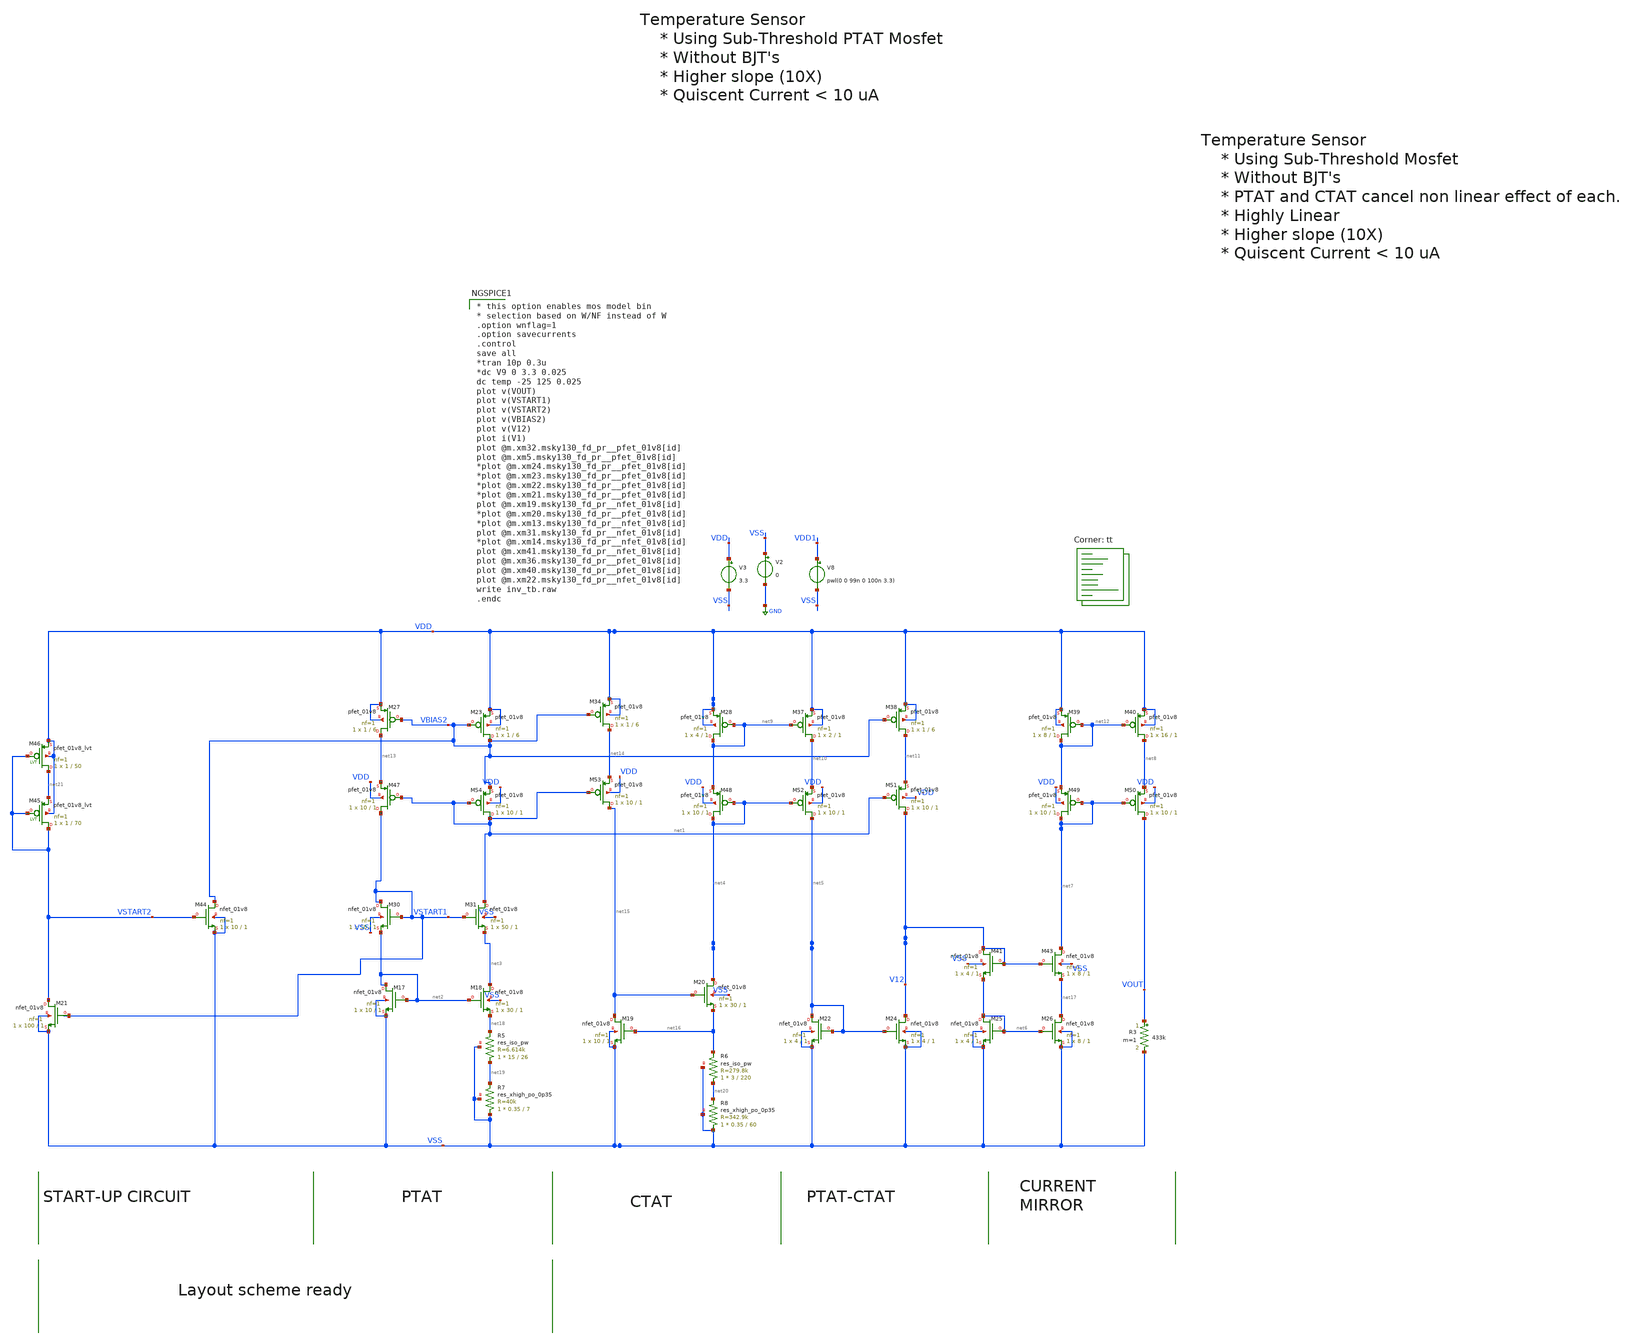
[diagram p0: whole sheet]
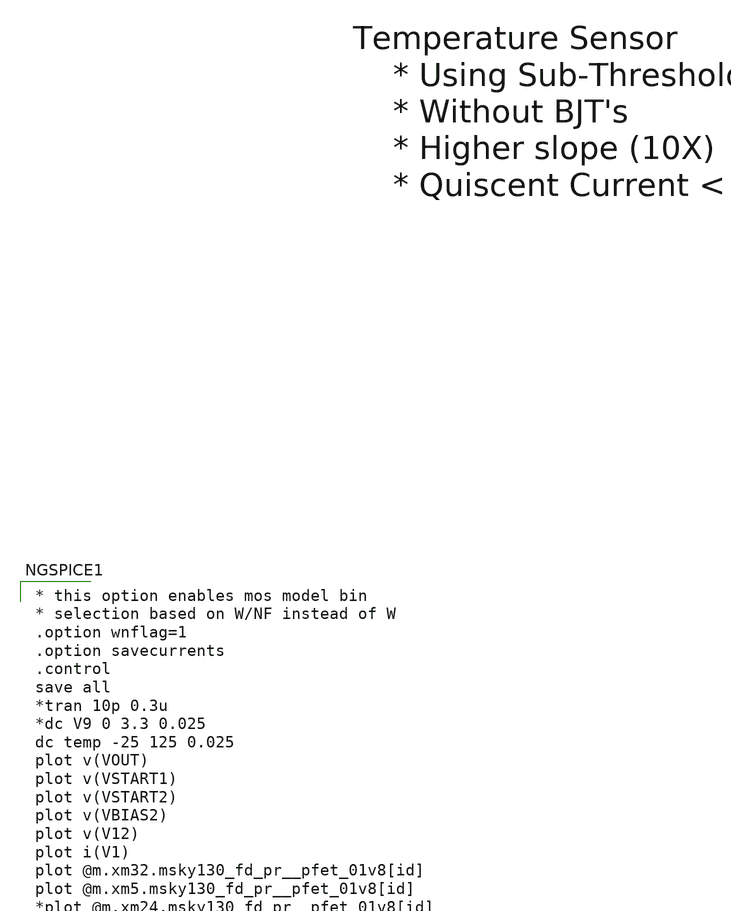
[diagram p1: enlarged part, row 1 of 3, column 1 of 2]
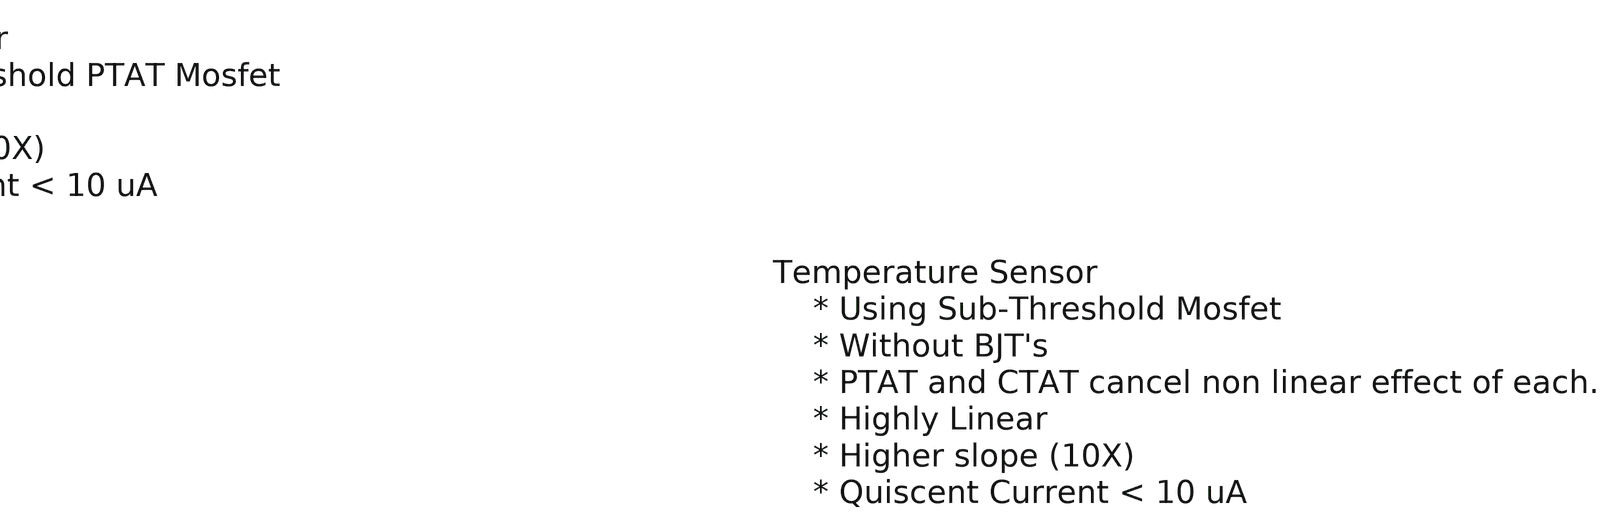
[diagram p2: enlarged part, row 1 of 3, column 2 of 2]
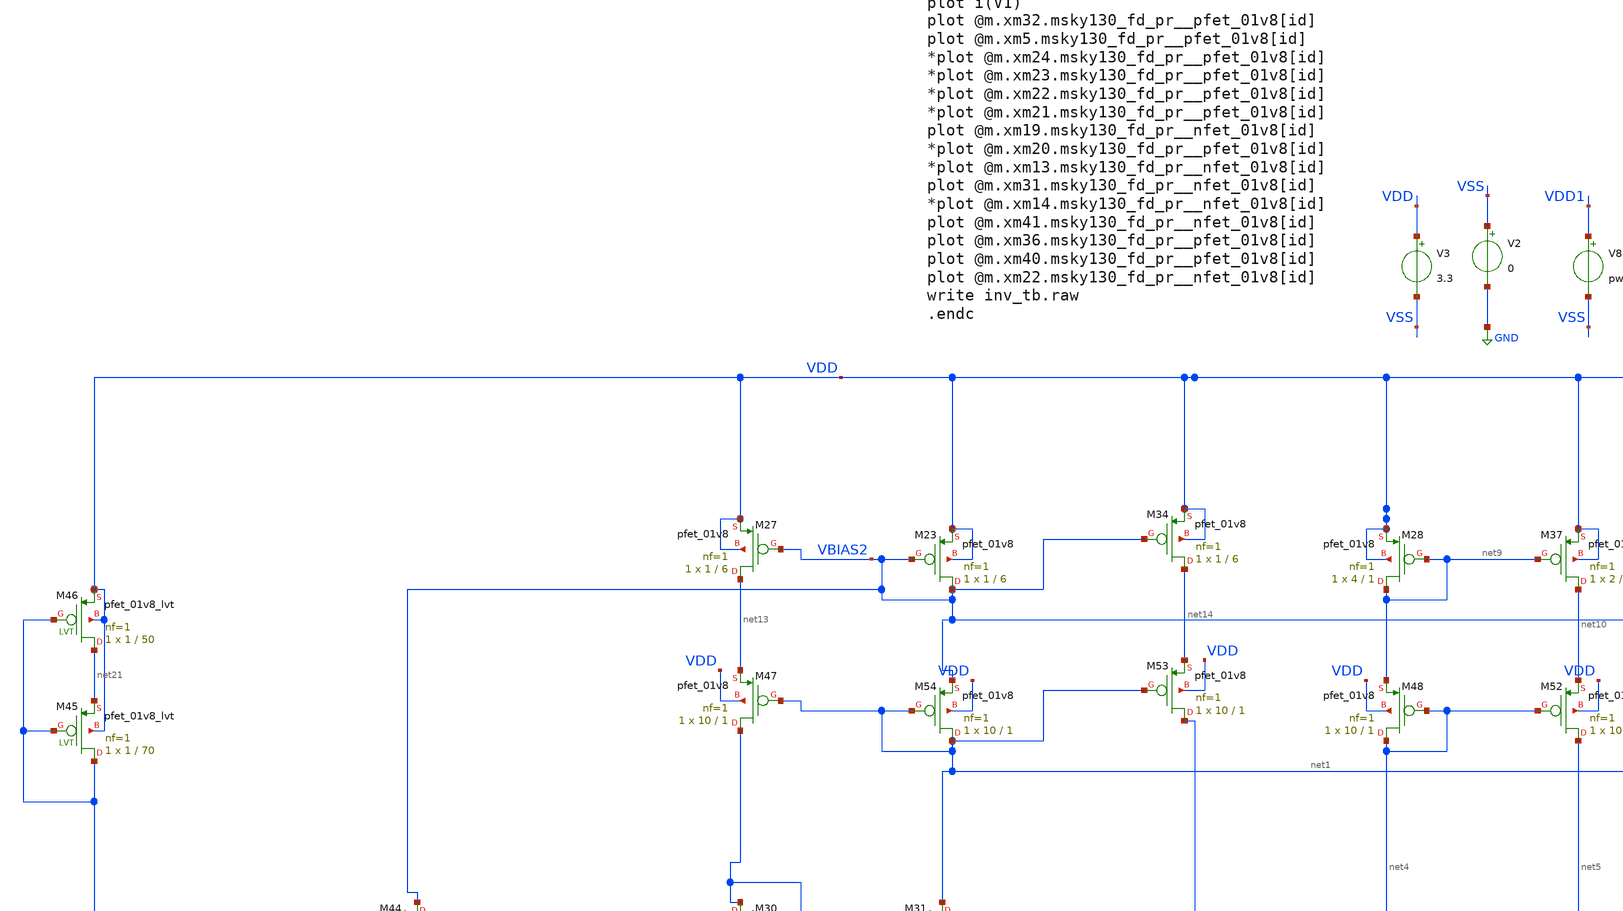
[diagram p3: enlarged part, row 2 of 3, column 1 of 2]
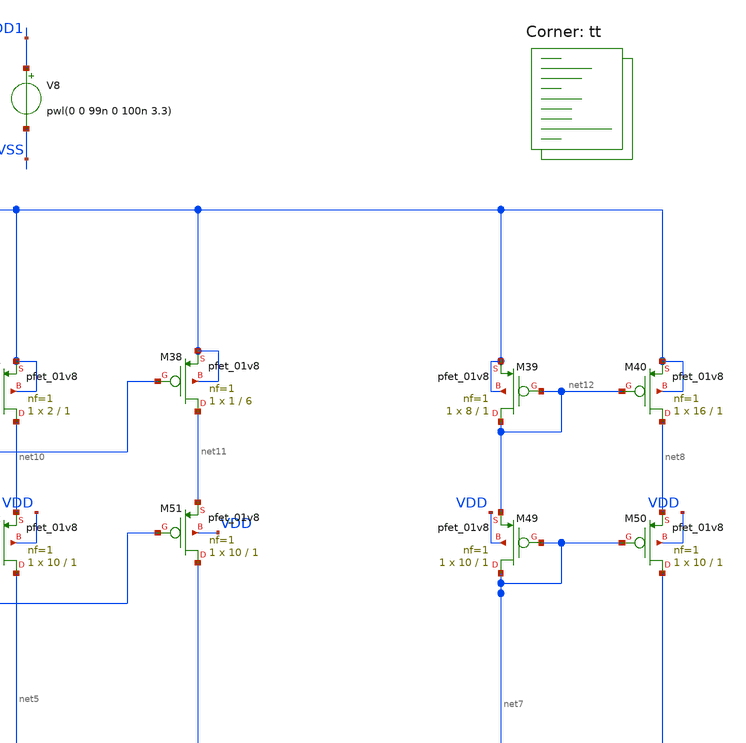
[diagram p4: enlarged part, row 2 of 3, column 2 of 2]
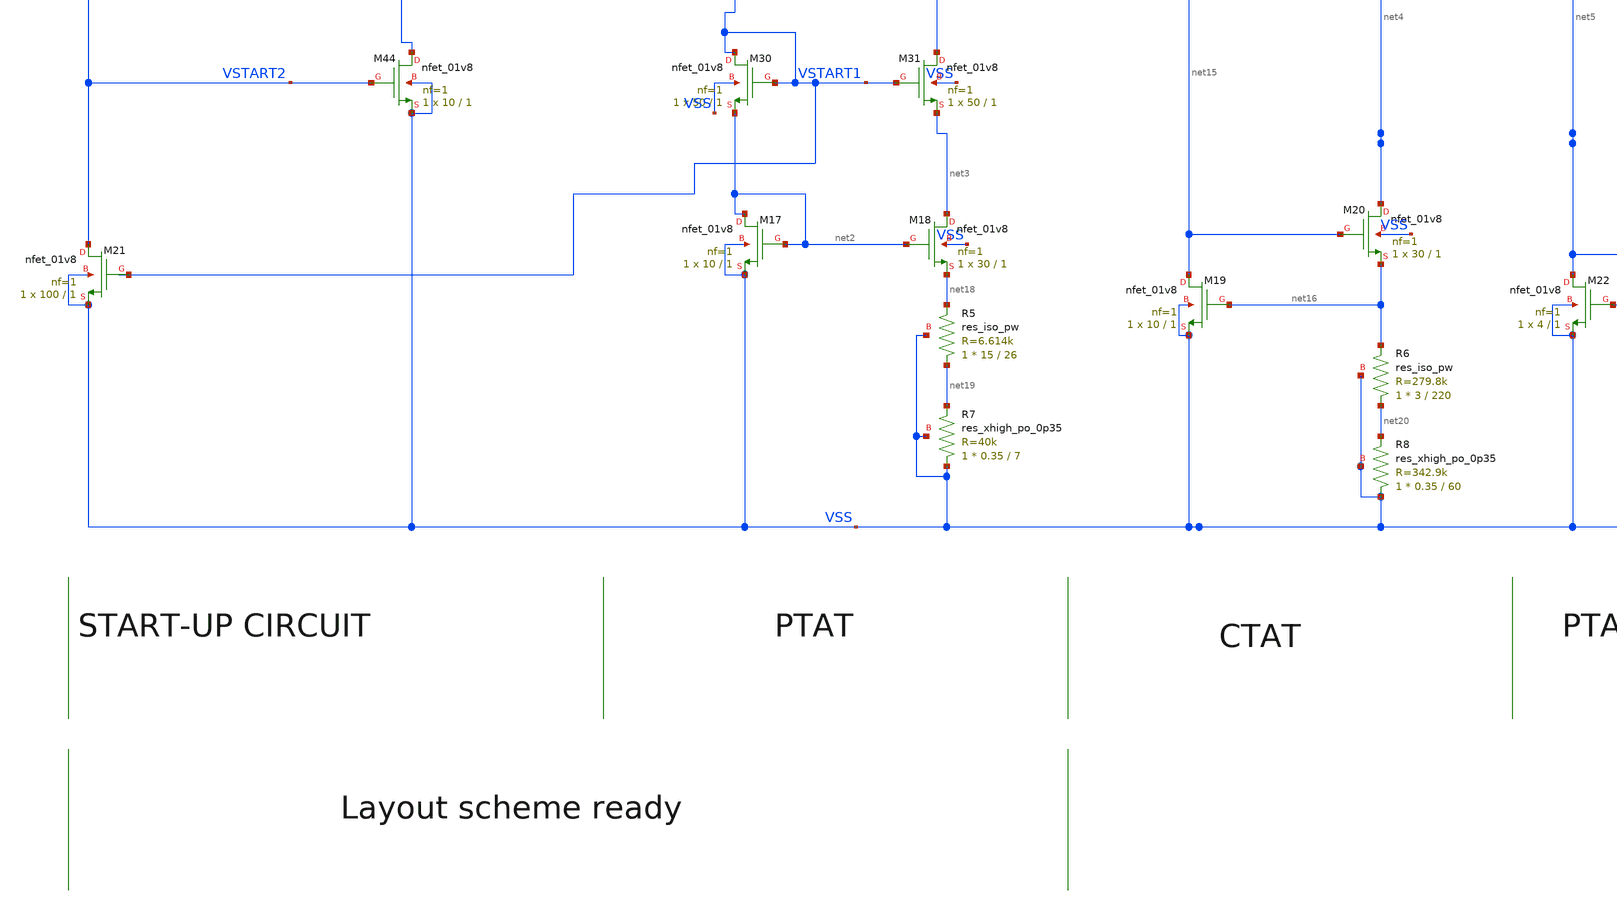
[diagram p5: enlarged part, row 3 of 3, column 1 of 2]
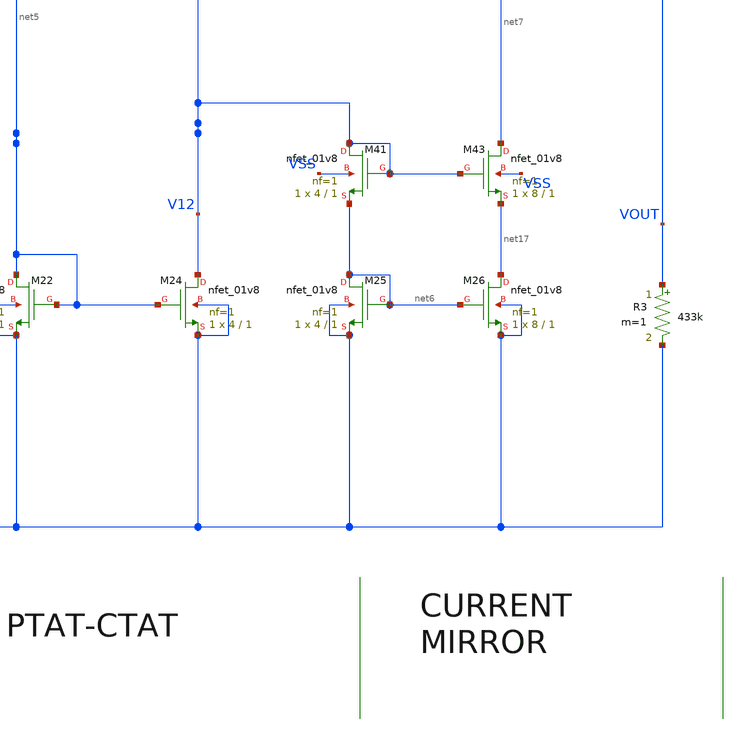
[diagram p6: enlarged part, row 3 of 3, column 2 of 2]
** sch_path: temp_sensor_finalized.sch
**.subckt temp_sensor_finalized
V2 VSS GND 0
V8 VDD1 VSS pwl(0 0 99n 0 100n 3.3)
XM17 net2 net2 VSS VSS sky130_fd_pr__nfet_01v8 L=1 W=10 nf=1 ad='int((nf+1)/2) * W/nf * 0.29' as='int((nf+2)/2) * W/nf * 0.29'
+ pd='2*int((nf+1)/2) * (W/nf + 0.29)' ps='2*int((nf+2)/2) * (W/nf + 0.29)' nrd='0.29 / W' nrs='0.29 / W'
+ sa=0 sb=0 sd=0 mult=1 m=1
XM18 net3 net2 net18 VSS sky130_fd_pr__nfet_01v8 L=1 W=30 nf=1 ad='int((nf+1)/2) * W/nf * 0.29' as='int((nf+2)/2) * W/nf * 0.29'
+ pd='2*int((nf+1)/2) * (W/nf + 0.29)' ps='2*int((nf+2)/2) * (W/nf + 0.29)' nrd='0.29 / W' nrs='0.29 / W'
+ sa=0 sb=0 sd=0 mult=1 m=1
XM19 net15 net16 VSS VSS sky130_fd_pr__nfet_01v8 L=1 W=10 nf=1 ad='int((nf+1)/2) * W/nf * 0.29' as='int((nf+2)/2) * W/nf * 0.29'
+ pd='2*int((nf+1)/2) * (W/nf + 0.29)' ps='2*int((nf+2)/2) * (W/nf + 0.29)' nrd='0.29 / W' nrs='0.29 / W'
+ sa=0 sb=0 sd=0 mult=1 m=1
XM20 net4 net15 net16 VSS sky130_fd_pr__nfet_01v8 L=1 W=30 nf=1 ad='int((nf+1)/2) * W/nf * 0.29' as='int((nf+2)/2) * W/nf * 0.29'
+ pd='2*int((nf+1)/2) * (W/nf + 0.29)' ps='2*int((nf+2)/2) * (W/nf + 0.29)' nrd='0.29 / W' nrs='0.29 / W'
+ sa=0 sb=0 sd=0 mult=1 m=1
XM22 net5 net5 VSS VSS sky130_fd_pr__nfet_01v8 L=1 W=4 nf=1 ad='int((nf+1)/2) * W/nf * 0.29' as='int((nf+2)/2) * W/nf * 0.29'
+ pd='2*int((nf+1)/2) * (W/nf + 0.29)' ps='2*int((nf+2)/2) * (W/nf + 0.29)' nrd='0.29 / W' nrs='0.29 / W'
+ sa=0 sb=0 sd=0 mult=1 m=1
XM24 V12 net5 VSS VSS sky130_fd_pr__nfet_01v8 L=1 W=4 nf=1 ad='int((nf+1)/2) * W/nf * 0.29' as='int((nf+2)/2) * W/nf * 0.29'
+ pd='2*int((nf+1)/2) * (W/nf + 0.29)' ps='2*int((nf+2)/2) * (W/nf + 0.29)' nrd='0.29 / W' nrs='0.29 / W'
+ sa=0 sb=0 sd=0 mult=1 m=1
XM25 net6 net6 VSS VSS sky130_fd_pr__nfet_01v8 L=1 W=4 nf=1 ad='int((nf+1)/2) * W/nf * 0.29' as='int((nf+2)/2) * W/nf * 0.29'
+ pd='2*int((nf+1)/2) * (W/nf + 0.29)' ps='2*int((nf+2)/2) * (W/nf + 0.29)' nrd='0.29 / W' nrs='0.29 / W'
+ sa=0 sb=0 sd=0 mult=1 m=1
XM26 net17 net6 VSS VSS sky130_fd_pr__nfet_01v8 L=1 W=8 nf=1 ad='int((nf+1)/2) * W/nf * 0.29' as='int((nf+2)/2) * W/nf * 0.29'
+ pd='2*int((nf+1)/2) * (W/nf + 0.29)' ps='2*int((nf+2)/2) * (W/nf + 0.29)' nrd='0.29 / W' nrs='0.29 / W'
+ sa=0 sb=0 sd=0 mult=1 m=1
V3 VDD VSS 3.3
XM21 VSTART2 VSTART1 VSS VSS sky130_fd_pr__nfet_01v8 L=1 W=100 nf=1 ad='int((nf+1)/2) * W/nf * 0.29'
+ as='int((nf+2)/2) * W/nf * 0.29' pd='2*int((nf+1)/2) * (W/nf + 0.29)' ps='2*int((nf+2)/2) * (W/nf + 0.29)'
+ nrd='0.29 / W' nrs='0.29 / W' sa=0 sb=0 sd=0 mult=1 m=1
XM30 VSTART1 VSTART1 net2 VSS sky130_fd_pr__nfet_01v8 L=1 W=50 nf=1 ad='int((nf+1)/2) * W/nf * 0.29'
+ as='int((nf+2)/2) * W/nf * 0.29' pd='2*int((nf+1)/2) * (W/nf + 0.29)' ps='2*int((nf+2)/2) * (W/nf + 0.29)'
+ nrd='0.29 / W' nrs='0.29 / W' sa=0 sb=0 sd=0 mult=1 m=1
XM31 net1 VSTART1 net3 VSS sky130_fd_pr__nfet_01v8 L=1 W=50 nf=1 ad='int((nf+1)/2) * W/nf * 0.29' as='int((nf+2)/2) * W/nf * 0.29'
+ pd='2*int((nf+1)/2) * (W/nf + 0.29)' ps='2*int((nf+2)/2) * (W/nf + 0.29)' nrd='0.29 / W' nrs='0.29 / W'
+ sa=0 sb=0 sd=0 mult=1 m=1
XM23 VBIAS2 VBIAS2 VDD VDD sky130_fd_pr__pfet_01v8 L=6 W=1 nf=1 ad='int((nf+1)/2) * W/nf * 0.29' as='int((nf+2)/2) * W/nf * 0.29'
+ pd='2*int((nf+1)/2) * (W/nf + 0.29)' ps='2*int((nf+2)/2) * (W/nf + 0.29)' nrd='0.29 / W' nrs='0.29 / W'
+ sa=0 sb=0 sd=0 mult=1 m=1
XM27 net13 VBIAS2 VDD VDD sky130_fd_pr__pfet_01v8 L=6 W=1 nf=1 ad='int((nf+1)/2) * W/nf * 0.29' as='int((nf+2)/2) * W/nf * 0.29'
+ pd='2*int((nf+1)/2) * (W/nf + 0.29)' ps='2*int((nf+2)/2) * (W/nf + 0.29)' nrd='0.29 / W' nrs='0.29 / W'
+ sa=0 sb=0 sd=0 mult=1 m=1
XM34 net14 VBIAS2 VDD VDD sky130_fd_pr__pfet_01v8 L=6 W=1 nf=1 ad='int((nf+1)/2) * W/nf * 0.29' as='int((nf+2)/2) * W/nf * 0.29'
+ pd='2*int((nf+1)/2) * (W/nf + 0.29)' ps='2*int((nf+2)/2) * (W/nf + 0.29)' nrd='0.29 / W' nrs='0.29 / W'
+ sa=0 sb=0 sd=0 mult=1 m=1
XM28 net9 net9 VDD VDD sky130_fd_pr__pfet_01v8 L=1 W=4 nf=1 ad='int((nf+1)/2) * W/nf * 0.29' as='int((nf+2)/2) * W/nf * 0.29'
+ pd='2*int((nf+1)/2) * (W/nf + 0.29)' ps='2*int((nf+2)/2) * (W/nf + 0.29)' nrd='0.29 / W' nrs='0.29 / W'
+ sa=0 sb=0 sd=0 mult=1 m=1
XM37 net10 net9 VDD VDD sky130_fd_pr__pfet_01v8 L=1 W=2 nf=1 ad='int((nf+1)/2) * W/nf * 0.29' as='int((nf+2)/2) * W/nf * 0.29'
+ pd='2*int((nf+1)/2) * (W/nf + 0.29)' ps='2*int((nf+2)/2) * (W/nf + 0.29)' nrd='0.29 / W' nrs='0.29 / W'
+ sa=0 sb=0 sd=0 mult=1 m=1
XM38 net11 VBIAS2 VDD VDD sky130_fd_pr__pfet_01v8 L=6 W=1 nf=1 ad='int((nf+1)/2) * W/nf * 0.29' as='int((nf+2)/2) * W/nf * 0.29'
+ pd='2*int((nf+1)/2) * (W/nf + 0.29)' ps='2*int((nf+2)/2) * (W/nf + 0.29)' nrd='0.29 / W' nrs='0.29 / W'
+ sa=0 sb=0 sd=0 mult=1 m=1
XM39 net12 net12 VDD VDD sky130_fd_pr__pfet_01v8 L=1 W=8 nf=1 ad='int((nf+1)/2) * W/nf * 0.29' as='int((nf+2)/2) * W/nf * 0.29'
+ pd='2*int((nf+1)/2) * (W/nf + 0.29)' ps='2*int((nf+2)/2) * (W/nf + 0.29)' nrd='0.29 / W' nrs='0.29 / W'
+ sa=0 sb=0 sd=0 mult=1 m=1
XM40 net8 net12 VDD VDD sky130_fd_pr__pfet_01v8 L=1 W=16 nf=1 ad='int((nf+1)/2) * W/nf * 0.29' as='int((nf+2)/2) * W/nf * 0.29'
+ pd='2*int((nf+1)/2) * (W/nf + 0.29)' ps='2*int((nf+2)/2) * (W/nf + 0.29)' nrd='0.29 / W' nrs='0.29 / W'
+ sa=0 sb=0 sd=0 mult=1 m=1
XM41 V12 V12 net6 VSS sky130_fd_pr__nfet_01v8 L=1 W=4 nf=1 ad='int((nf+1)/2) * W/nf * 0.29' as='int((nf+2)/2) * W/nf * 0.29'
+ pd='2*int((nf+1)/2) * (W/nf + 0.29)' ps='2*int((nf+2)/2) * (W/nf + 0.29)' nrd='0.29 / W' nrs='0.29 / W'
+ sa=0 sb=0 sd=0 mult=1 m=1
XM43 net7 V12 net17 VSS sky130_fd_pr__nfet_01v8 L=1 W=8 nf=1 ad='int((nf+1)/2) * W/nf * 0.29' as='int((nf+2)/2) * W/nf * 0.29'
+ pd='2*int((nf+1)/2) * (W/nf + 0.29)' ps='2*int((nf+2)/2) * (W/nf + 0.29)' nrd='0.29 / W' nrs='0.29 / W'
+ sa=0 sb=0 sd=0 mult=1 m=1
XM44 VBIAS2 VSTART2 VSS VSS sky130_fd_pr__nfet_01v8 L=1 W=10 nf=1 ad='int((nf+1)/2) * W/nf * 0.29' as='int((nf+2)/2) * W/nf * 0.29'
+ pd='2*int((nf+1)/2) * (W/nf + 0.29)' ps='2*int((nf+2)/2) * (W/nf + 0.29)' nrd='0.29 / W' nrs='0.29 / W'
+ sa=0 sb=0 sd=0 mult=1 m=1
R3 VOUT VSS 433k m=1
XR5 net19 net18 VSS sky130_fd_pr__res_iso_pw W=15 L=26 m=1
XR6 net20 net16 VSS sky130_fd_pr__res_iso_pw W=3 L=220 m=1
XM45 VSTART2 VSTART2 net21 VDD sky130_fd_pr__pfet_01v8_lvt L=70 W=1 nf=1 ad='int((nf+1)/2) * W/nf * 0.29'
+ as='int((nf+2)/2) * W/nf * 0.29' pd='2*int((nf+1)/2) * (W/nf + 0.29)' ps='2*int((nf+2)/2) * (W/nf + 0.29)'
+ nrd='0.29 / W' nrs='0.29 / W' sa=0 sb=0 sd=0 mult=1 m=1
XM46 net21 VSTART2 VDD VDD sky130_fd_pr__pfet_01v8_lvt L=50 W=1 nf=1 ad='int((nf+1)/2) * W/nf * 0.29'
+ as='int((nf+2)/2) * W/nf * 0.29' pd='2*int((nf+1)/2) * (W/nf + 0.29)' ps='2*int((nf+2)/2) * (W/nf + 0.29)'
+ nrd='0.29 / W' nrs='0.29 / W' sa=0 sb=0 sd=0 mult=1 m=1
XM47 VSTART1 net1 net13 VDD sky130_fd_pr__pfet_01v8 L=1 W=10 nf=1 ad='int((nf+1)/2) * W/nf * 0.29' as='int((nf+2)/2) * W/nf * 0.29'
+ pd='2*int((nf+1)/2) * (W/nf + 0.29)' ps='2*int((nf+2)/2) * (W/nf + 0.29)' nrd='0.29 / W' nrs='0.29 / W'
+ sa=0 sb=0 sd=0 mult=1 m=1
XM48 net4 net4 net9 VDD sky130_fd_pr__pfet_01v8 L=1 W=10 nf=1 ad='int((nf+1)/2) * W/nf * 0.29' as='int((nf+2)/2) * W/nf * 0.29'
+ pd='2*int((nf+1)/2) * (W/nf + 0.29)' ps='2*int((nf+2)/2) * (W/nf + 0.29)' nrd='0.29 / W' nrs='0.29 / W'
+ sa=0 sb=0 sd=0 mult=1 m=1
XM49 net7 net7 net12 VDD sky130_fd_pr__pfet_01v8 L=1 W=10 nf=1 ad='int((nf+1)/2) * W/nf * 0.29' as='int((nf+2)/2) * W/nf * 0.29'
+ pd='2*int((nf+1)/2) * (W/nf + 0.29)' ps='2*int((nf+2)/2) * (W/nf + 0.29)' nrd='0.29 / W' nrs='0.29 / W'
+ sa=0 sb=0 sd=0 mult=1 m=1
XM50 VOUT net7 net8 VDD sky130_fd_pr__pfet_01v8 L=1 W=10 nf=1 ad='int((nf+1)/2) * W/nf * 0.29' as='int((nf+2)/2) * W/nf * 0.29'
+ pd='2*int((nf+1)/2) * (W/nf + 0.29)' ps='2*int((nf+2)/2) * (W/nf + 0.29)' nrd='0.29 / W' nrs='0.29 / W'
+ sa=0 sb=0 sd=0 mult=1 m=1
XM51 V12 net1 net11 VDD sky130_fd_pr__pfet_01v8 L=1 W=10 nf=1 ad='int((nf+1)/2) * W/nf * 0.29' as='int((nf+2)/2) * W/nf * 0.29'
+ pd='2*int((nf+1)/2) * (W/nf + 0.29)' ps='2*int((nf+2)/2) * (W/nf + 0.29)' nrd='0.29 / W' nrs='0.29 / W'
+ sa=0 sb=0 sd=0 mult=1 m=1
XM52 net5 net4 net10 VDD sky130_fd_pr__pfet_01v8 L=1 W=10 nf=1 ad='int((nf+1)/2) * W/nf * 0.29' as='int((nf+2)/2) * W/nf * 0.29'
+ pd='2*int((nf+1)/2) * (W/nf + 0.29)' ps='2*int((nf+2)/2) * (W/nf + 0.29)' nrd='0.29 / W' nrs='0.29 / W'
+ sa=0 sb=0 sd=0 mult=1 m=1
XM53 net15 net1 net14 VDD sky130_fd_pr__pfet_01v8 L=1 W=10 nf=1 ad='int((nf+1)/2) * W/nf * 0.29' as='int((nf+2)/2) * W/nf * 0.29'
+ pd='2*int((nf+1)/2) * (W/nf + 0.29)' ps='2*int((nf+2)/2) * (W/nf + 0.29)' nrd='0.29 / W' nrs='0.29 / W'
+ sa=0 sb=0 sd=0 mult=1 m=1
XM54 net1 net1 VBIAS2 VDD sky130_fd_pr__pfet_01v8 L=1 W=10 nf=1 ad='int((nf+1)/2) * W/nf * 0.29' as='int((nf+2)/2) * W/nf * 0.29'
+ pd='2*int((nf+1)/2) * (W/nf + 0.29)' ps='2*int((nf+2)/2) * (W/nf + 0.29)' nrd='0.29 / W' nrs='0.29 / W'
+ sa=0 sb=0 sd=0 mult=1 m=1
XR7 VSS net19 VSS sky130_fd_pr__res_xhigh_po_0p35 L=7 mult=1 m=1
XR8 VSS net20 VSS sky130_fd_pr__res_xhigh_po_0p35 L=60 mult=1 m=1
**** begin user architecture code

* this option enables mos model bin
* selection based on W/NF instead of W
.option wnflag=1
.option savecurrents
.control
save all
*tran 10p 0.3u
*dc V9 0 3.3 0.025
dc temp -25 125 0.025
plot v(VOUT)
plot v(VSTART1)
plot v(VSTART2)
plot v(VBIAS2)
plot v(V12)
plot i(V1)
plot @m.xm32.msky130_fd_pr__pfet_01v8[id]
plot @m.xm5.msky130_fd_pr__pfet_01v8[id]
*plot @m.xm24.msky130_fd_pr__pfet_01v8[id]
*plot @m.xm23.msky130_fd_pr__pfet_01v8[id]
*plot @m.xm22.msky130_fd_pr__pfet_01v8[id]
*plot @m.xm21.msky130_fd_pr__pfet_01v8[id]
plot @m.xm19.msky130_fd_pr__nfet_01v8[id]
*plot @m.xm20.msky130_fd_pr__pfet_01v8[id]
*plot @m.xm13.msky130_fd_pr__nfet_01v8[id]
plot @m.xm31.msky130_fd_pr__nfet_01v8[id]
*plot @m.xm14.msky130_fd_pr__nfet_01v8[id]
plot @m.xm41.msky130_fd_pr__nfet_01v8[id]
plot @m.xm36.msky130_fd_pr__pfet_01v8[id]
plot @m.xm40.msky130_fd_pr__pfet_01v8[id]
plot @m.xm22.msky130_fd_pr__nfet_01v8[id]
write inv_tb.raw
.endc


.lib $::SKYWATER_MODELS/sky130.lib.spice tt
**** end user architecture code
**.ends
.GLOBAL GND
.end
